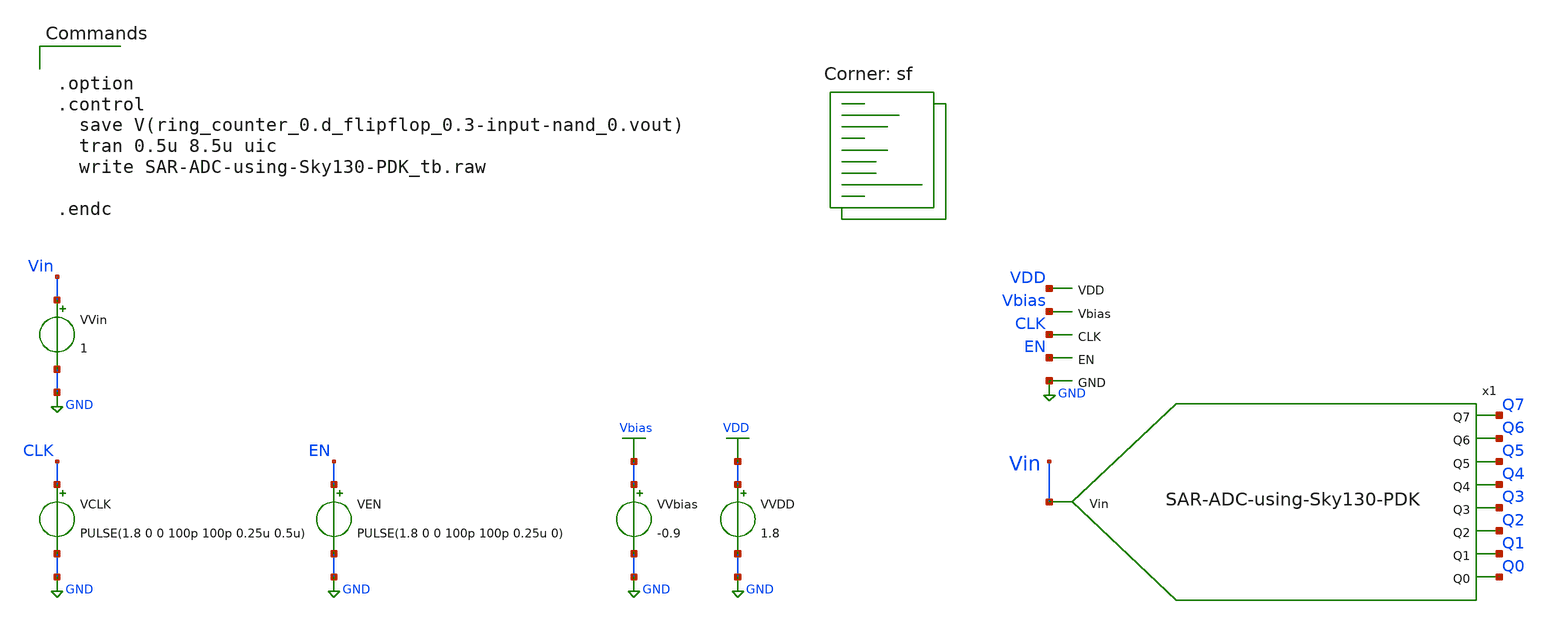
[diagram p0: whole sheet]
** sch_path: xschem/SAR-ADC-using-Sky130-PDK_tb.sch
**.subckt SAR-ADC-using-Sky130-PDK_tb
x1 VDD Vin Q0 Vbias EN Q1 CLK Q2 Q3 Q4 Q5 Q6 Q7 GND SAR-ADC-using-Sky130-PDK
VCLK CLK GND PULSE(1.8 0 0 100p 100p 0.25u 0.5u)
VVDD VDD GND 1.8
VEN EN GND PULSE(1.8 0 0 100p 100p 0.25u 0)
VVbias Vbias GND -0.9
VVin Vin GND 1
**** begin user architecture code


.option
.control
  save V(ring_counter_0.d_flipflop_0.3-input-nand_0.vout)
  tran 0.5u 8.5u uic
  write SAR-ADC-using-Sky130-PDK_tb.raw

.endc


.lib $::SKYWATER_MODELS/sky130.lib.spice sf
**** end user architecture code
**.ends
.GLOBAL GND
.GLOBAL VDD
.GLOBAL Vbias
.end
